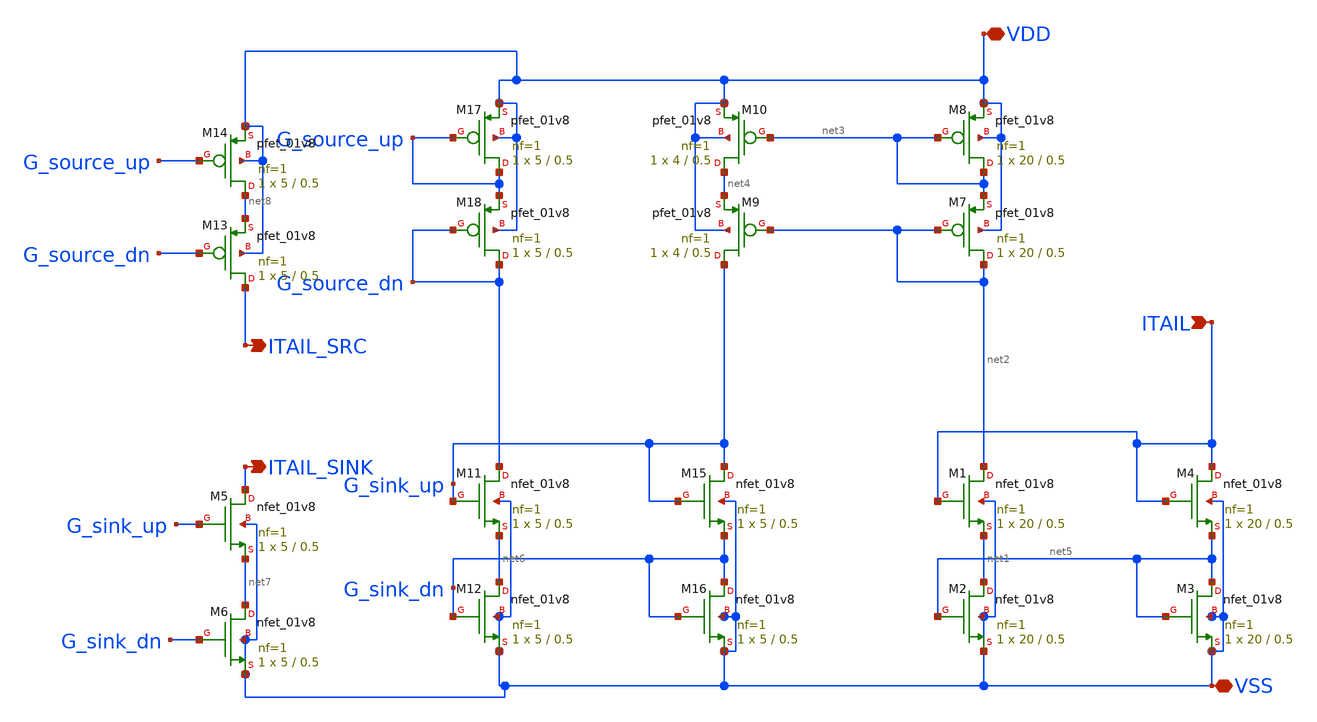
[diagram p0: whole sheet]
** sch_path: Xschem/TOP/Current_Mirror_Top_s.sch
**.subckt Current_Mirror_Top_s ITAIL VDD VSS ITAIL_SRC ITAIL_SINK
*.ipin ITAIL
*.iopin VDD
*.iopin VSS
*.opin ITAIL_SRC
*.opin ITAIL_SINK
XM5 ITAIL_SINK G_sink_up net7 VSS sky130_fd_pr__nfet_01v8 L=0.5 W=5 nf=1 ad='int((nf+1)/2) * W/nf * 0.29'
+ as='int((nf+2)/2) * W/nf * 0.29' pd='2*int((nf+1)/2) * (W/nf + 0.29)' ps='2*int((nf+2)/2) * (W/nf + 0.29)'
+ nrd='0.29 / W' nrs='0.29 / W' sa=0 sb=0 sd=0 mult=1 m=1
XM6 net7 G_sink_dn VSS VSS sky130_fd_pr__nfet_01v8 L=0.5 W=5 nf=1 ad='int((nf+1)/2) * W/nf * 0.29' as='int((nf+2)/2) * W/nf * 0.29'
+ pd='2*int((nf+1)/2) * (W/nf + 0.29)' ps='2*int((nf+2)/2) * (W/nf + 0.29)' nrd='0.29 / W' nrs='0.29 / W'
+ sa=0 sb=0 sd=0 mult=1 m=1
XM11 G_source_dn G_sink_up net6 VSS sky130_fd_pr__nfet_01v8 L=0.5 W=5 nf=1 ad='int((nf+1)/2) * W/nf * 0.29'
+ as='int((nf+2)/2) * W/nf * 0.29' pd='2*int((nf+1)/2) * (W/nf + 0.29)' ps='2*int((nf+2)/2) * (W/nf + 0.29)'
+ nrd='0.29 / W' nrs='0.29 / W' sa=0 sb=0 sd=0 mult=1 m=1
XM12 net6 G_sink_dn VSS VSS sky130_fd_pr__nfet_01v8 L=0.5 W=5 nf=1 ad='int((nf+1)/2) * W/nf * 0.29' as='int((nf+2)/2) * W/nf * 0.29'
+ pd='2*int((nf+1)/2) * (W/nf + 0.29)' ps='2*int((nf+2)/2) * (W/nf + 0.29)' nrd='0.29 / W' nrs='0.29 / W'
+ sa=0 sb=0 sd=0 mult=1 m=1
XM15 G_sink_up G_sink_up G_sink_dn VSS sky130_fd_pr__nfet_01v8 L=0.5 W=5 nf=1 ad='int((nf+1)/2) * W/nf * 0.29'
+ as='int((nf+2)/2) * W/nf * 0.29' pd='2*int((nf+1)/2) * (W/nf + 0.29)' ps='2*int((nf+2)/2) * (W/nf + 0.29)'
+ nrd='0.29 / W' nrs='0.29 / W' sa=0 sb=0 sd=0 mult=1 m=1
XM16 G_sink_dn G_sink_dn VSS VSS sky130_fd_pr__nfet_01v8 L=0.5 W=5 nf=1 ad='int((nf+1)/2) * W/nf * 0.29'
+ as='int((nf+2)/2) * W/nf * 0.29' pd='2*int((nf+1)/2) * (W/nf + 0.29)' ps='2*int((nf+2)/2) * (W/nf + 0.29)'
+ nrd='0.29 / W' nrs='0.29 / W' sa=0 sb=0 sd=0 mult=1 m=1
XM1 net2 ITAIL net1 VSS sky130_fd_pr__nfet_01v8 L=0.5 W=20 nf=1 ad='int((nf+1)/2) * W/nf * 0.29' as='int((nf+2)/2) * W/nf * 0.29'
+ pd='2*int((nf+1)/2) * (W/nf + 0.29)' ps='2*int((nf+2)/2) * (W/nf + 0.29)' nrd='0.29 / W' nrs='0.29 / W'
+ sa=0 sb=0 sd=0 mult=1 m=1
XM2 net1 net5 VSS VSS sky130_fd_pr__nfet_01v8 L=0.5 W=20 nf=1 ad='int((nf+1)/2) * W/nf * 0.29' as='int((nf+2)/2) * W/nf * 0.29'
+ pd='2*int((nf+1)/2) * (W/nf + 0.29)' ps='2*int((nf+2)/2) * (W/nf + 0.29)' nrd='0.29 / W' nrs='0.29 / W'
+ sa=0 sb=0 sd=0 mult=1 m=1
XM3 net5 net5 VSS VSS sky130_fd_pr__nfet_01v8 L=0.5 W=20 nf=1 ad='int((nf+1)/2) * W/nf * 0.29' as='int((nf+2)/2) * W/nf * 0.29'
+ pd='2*int((nf+1)/2) * (W/nf + 0.29)' ps='2*int((nf+2)/2) * (W/nf + 0.29)' nrd='0.29 / W' nrs='0.29 / W'
+ sa=0 sb=0 sd=0 mult=1 m=1
XM4 ITAIL ITAIL net5 VSS sky130_fd_pr__nfet_01v8 L=0.5 W=20 nf=1 ad='int((nf+1)/2) * W/nf * 0.29' as='int((nf+2)/2) * W/nf * 0.29'
+ pd='2*int((nf+1)/2) * (W/nf + 0.29)' ps='2*int((nf+2)/2) * (W/nf + 0.29)' nrd='0.29 / W' nrs='0.29 / W'
+ sa=0 sb=0 sd=0 mult=1 m=1
XM13 ITAIL_SRC G_source_dn net8 VDD sky130_fd_pr__pfet_01v8 L=0.5 W=5 nf=1 ad='int((nf+1)/2) * W/nf * 0.29'
+ as='int((nf+2)/2) * W/nf * 0.29' pd='2*int((nf+1)/2) * (W/nf + 0.29)' ps='2*int((nf+2)/2) * (W/nf + 0.29)'
+ nrd='0.29 / W' nrs='0.29 / W' sa=0 sb=0 sd=0 mult=1 m=1
XM14 net8 G_source_up VDD VDD sky130_fd_pr__pfet_01v8 L=0.5 W=5 nf=1 ad='int((nf+1)/2) * W/nf * 0.29'
+ as='int((nf+2)/2) * W/nf * 0.29' pd='2*int((nf+1)/2) * (W/nf + 0.29)' ps='2*int((nf+2)/2) * (W/nf + 0.29)'
+ nrd='0.29 / W' nrs='0.29 / W' sa=0 sb=0 sd=0 mult=1 m=1
XM17 G_source_up G_source_up VDD VDD sky130_fd_pr__pfet_01v8 L=0.5 W=5 nf=1 ad='int((nf+1)/2) * W/nf * 0.29'
+ as='int((nf+2)/2) * W/nf * 0.29' pd='2*int((nf+1)/2) * (W/nf + 0.29)' ps='2*int((nf+2)/2) * (W/nf + 0.29)'
+ nrd='0.29 / W' nrs='0.29 / W' sa=0 sb=0 sd=0 mult=1 m=1
XM18 G_source_dn G_source_dn G_source_up VDD sky130_fd_pr__pfet_01v8 L=0.5 W=5 nf=1 ad='int((nf+1)/2) * W/nf * 0.29'
+ as='int((nf+2)/2) * W/nf * 0.29' pd='2*int((nf+1)/2) * (W/nf + 0.29)' ps='2*int((nf+2)/2) * (W/nf + 0.29)'
+ nrd='0.29 / W' nrs='0.29 / W' sa=0 sb=0 sd=0 mult=1 m=1
XM9 G_sink_up net2 net4 VDD sky130_fd_pr__pfet_01v8 L=0.5 W=4 nf=1 ad='int((nf+1)/2) * W/nf * 0.29' as='int((nf+2)/2) * W/nf * 0.29'
+ pd='2*int((nf+1)/2) * (W/nf + 0.29)' ps='2*int((nf+2)/2) * (W/nf + 0.29)' nrd='0.29 / W' nrs='0.29 / W'
+ sa=0 sb=0 sd=0 mult=1 m=1
XM10 net4 net3 VDD VDD sky130_fd_pr__pfet_01v8 L=0.5 W=4 nf=1 ad='int((nf+1)/2) * W/nf * 0.29' as='int((nf+2)/2) * W/nf * 0.29'
+ pd='2*int((nf+1)/2) * (W/nf + 0.29)' ps='2*int((nf+2)/2) * (W/nf + 0.29)' nrd='0.29 / W' nrs='0.29 / W'
+ sa=0 sb=0 sd=0 mult=1 m=1
XM7 net2 net2 net3 VDD sky130_fd_pr__pfet_01v8 L=0.5 W=20 nf=1 ad='int((nf+1)/2) * W/nf * 0.29' as='int((nf+2)/2) * W/nf * 0.29'
+ pd='2*int((nf+1)/2) * (W/nf + 0.29)' ps='2*int((nf+2)/2) * (W/nf + 0.29)' nrd='0.29 / W' nrs='0.29 / W'
+ sa=0 sb=0 sd=0 mult=1 m=1
XM8 net3 net3 VDD VDD sky130_fd_pr__pfet_01v8 L=0.5 W=20 nf=1 ad='int((nf+1)/2) * W/nf * 0.29' as='int((nf+2)/2) * W/nf * 0.29'
+ pd='2*int((nf+1)/2) * (W/nf + 0.29)' ps='2*int((nf+2)/2) * (W/nf + 0.29)' nrd='0.29 / W' nrs='0.29 / W'
+ sa=0 sb=0 sd=0 mult=1 m=1
**.ends
.end
